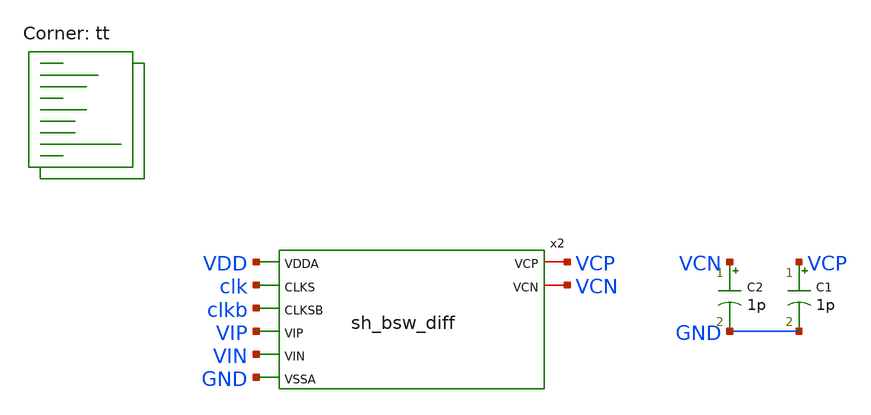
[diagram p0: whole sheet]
** sch_path: xschem/sh_bsw_diff-tb.sch
**.subckt sh_bsw_diff-tb
C1 VCP GND 1p m=1
x2 VDD clk clkb VIP VIN GND VCP VCN sh_bsw_diff
C2 VCN GND 1p m=1
**** begin user architecture code
 .lib $::SKYWATER_MODELS/sky130.lib.spice tt
.include $::SKYWATER_STDCELLS/sky130_fd_sc_hd.spice
.param mc_mm_switch = 0
.param mc_pr_switch = 0




  .param fin=9.3e3 in_delay={10e-9} in_period={1/fin} vcn_delay={in_period/2}
  .param fclk={20e3} tclk={1/fclk} thclk={tclk/2}
  .option wnflag=1
  .option safecurrents

  Vvdd   vdd   gnd 1.8
  Vdtp   vip   gnd sin(0.5 0.5 {fin} {in_delay})
  Vdtn   vin   gnd sin(0.5 0.5 {fin} {in_delay+vcn_delay})
  Vclk   clk   gnd pulse(0 1.8 10e-9 1p 1p {thclk} {tclk})
  Vclkb  clkb  gnd pulse(1.8 0 10e-9 1p 1p {thclk} {tclk})

  .control
     reset
     save all
     tran 10n 2m uic
     write sh_bsw_diff-tb.raw
    quit 0
  .endc



**** end user architecture code
**.ends
.end
